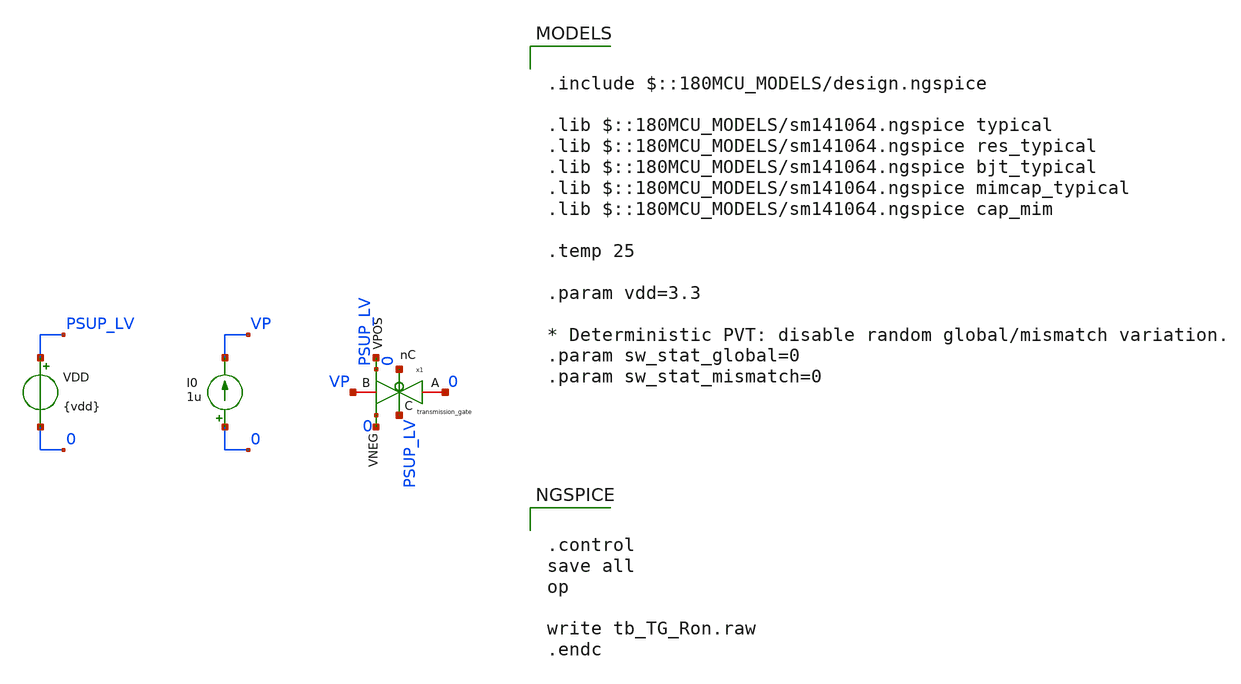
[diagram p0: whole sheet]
** sch_path: xschem/blocks/transmission_gate/tb_TG_Ron.sch
**.subckt tb_TG_Ron
x1 PSUP_LV 0 VP 0 net1 net2 transmission_gate
VDD PSUP_LV 0 {vdd}
I0 0 VP 1u
**** begin user architecture code

.include $::180MCU_MODELS/design.ngspice

.lib $::180MCU_MODELS/sm141064.ngspice typical
.lib $::180MCU_MODELS/sm141064.ngspice res_typical
.lib $::180MCU_MODELS/sm141064.ngspice bjt_typical
.lib $::180MCU_MODELS/sm141064.ngspice mimcap_typical
.lib $::180MCU_MODELS/sm141064.ngspice cap_mim

.temp 25

.param vdd=3.3

* Deterministic PVT: disable random global/mismatch variation.
.param sw_stat_global=0
.param sw_stat_mismatch=0



.control
save all
op

write tb_TG_Ron.raw
.endc


**** end user architecture code
**.ends

* expanding   symbol:  blocks/transmission_gate/transmission_gate.sym # of pins=6
** sym_path: xschem/blocks/transmission_gate/transmission_gate.sym
** sch_path: xschem/blocks/transmission_gate/transmission_gate.sch
.subckt transmission_gate C A B nC VPOS VNEG
*.iopin A
*.iopin B
*.ipin C
*.ipin nC
*.ipin VPOS
*.ipin VNEG
XM3 A C B VNEG nfet_03v3 L=2u W=10u nf=1 ad='int((nf+1)/2) * W/nf * 0.18u' as='int((nf+2)/2) * W/nf * 0.18u'
+ pd='2*int((nf+1)/2) * (W/nf + 0.18u)' ps='2*int((nf+2)/2) * (W/nf + 0.18u)' nrd='0.18u / W' nrs='0.18u / W'
+ sa=0 sb=0 sd=0 m=8
XM4 A nC B VPOS pfet_03v3 L=2u W=10u nf=1 ad='int((nf+1)/2) * W/nf * 0.18u' as='int((nf+2)/2) * W/nf * 0.18u'
+ pd='2*int((nf+1)/2) * (W/nf + 0.18u)' ps='2*int((nf+2)/2) * (W/nf + 0.18u)' nrd='0.18u / W' nrs='0.18u / W'
+ sa=0 sb=0 sd=0 m=16
.ends

.end
